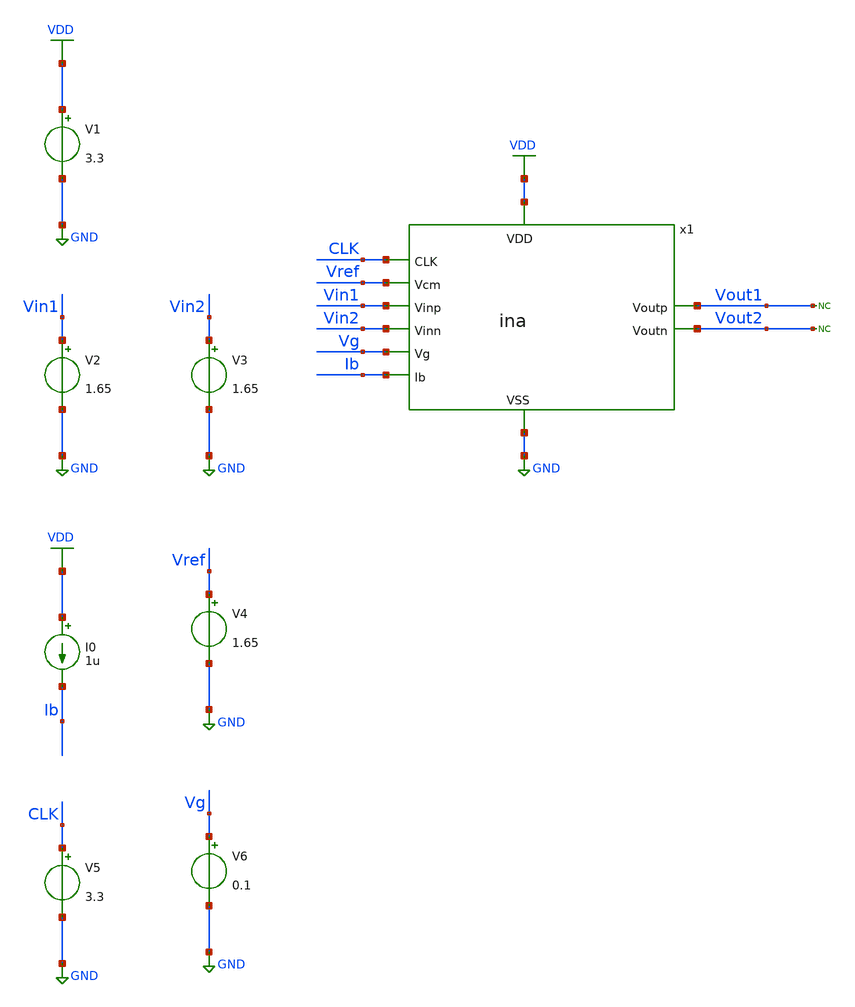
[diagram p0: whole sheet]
** sch_path: designs/libs/tb_ina/tb_ina_tran/tb_ina_tran.sch
**.subckt tb_ina_tran
V1 VDD GND 3.3
V2 Vin1 GND 1.65
V3 Vin2 GND 1.65
I0 VDD Ib 1u
V4 Vref GND 1.65
x1 Vg VDD Vin1 Vin2 CLK Vout1 Vout2 GND Vref Ib ina
V5 CLK GND 3.3
V6 Vg GND 0.1
* noconn Vout1
* noconn Vout2
**** begin user architecture code

.include $::180MCU_MODELS/design.ngspice
.lib $::180MCU_MODELS/sm141064.ngspice typical
.lib $::180MCU_MODELS/sm141064.ngspice cap_mim
.lib $::180MCU_MODELS/sm141064.ngspice moscap_typical
.lib $::180MCU_MODELS/sm141064.ngspice mimcap_typical
.lib $::180MCU_MODELS/sm141064.ngspice res_typical
* .lib $::180MCU_MODELS/sm141064.ngspice res_statistical
* ngspice commands




.control
save all

run
set color0 = white

*************************************
** ECG INPUT PARAMETERS
*************************************

let Vdd  = 3.3
let Vcm  = 1.65
let Vamp = 0.5m
let fecg = 100

*************************************
** CHOPPER PARAMETERS
*************************************

let fchop = 4k
let tper = 1/fchop
let ton = tper/2
let tr = 10n
let tf = 10n

*************************************
** BIAS PARAMETERS
*************************************

let Ibias = 2u
let Vref  = Vdd/2
let Vg 	  = 0.1

*************************************
** TRANSIENT PARAMETERS
*************************************

let tstop = 300m
let tstep = 10u

*************************************
** SOURCES
*************************************

alter @V1[DC] = $&Vdd
alter @V2[SIN] = [ $&Vcm $&Vamp $&fecg ]
alter @V3[SIN] = [ $&Vcm -$&Vamp $&fecg ]
alter @V4[DC] = $&Vref
alter @I0[DC] = $&Ibias
alter @V5[PULSE] = [ 0 $&Vdd 0 $&tr $&tf $&ton $&tper 0 ]
alter @V6[DC] = $&Vg

*************************************
** TRANSIENT SIMULATION
*************************************

tran $&tstep $&tstop

*************************************
** PLOTS
*************************************

setplot tran1
let vin1 = v(Vin1)
let vin2 = v(Vin2)
let vout1 = v(Vout1)
let vout2 = v(Vout2)
let vin_diff  = vin1-vin2
let vout_diff = vout1-vout2
let vcm_out = (vout1+vout2)/2
let vclk = v(CLK)
plot vclk xlimit 40m 41m
plot vin1 vin2
plot vin_diff
plot vout1 vout2
plot vout_diff
plot vin_diff vout_diff
plot vcm_out 1.65

*************************************
** MEASUREMENTS
*************************************

let tinit=tstop-40m
meas tran VCM_AVG AVG vcm_out FROM=tinit TO=tstop
meas tran VCM_MIN MIN vcm_out FROM=tinit TO=tstop
meas tran VCM_MAX MAX vcm_out FROM=tinit TO=tstop
print VCM_AVG
print VCM_MIN
print VCM_MAX

*************************************
** SAVE
*************************************

write tb_ina_tran.raw

.endc
* ngspice commands



**** end user architecture code
**.ends
.GLOBAL GND
.GLOBAL VDD
.end
